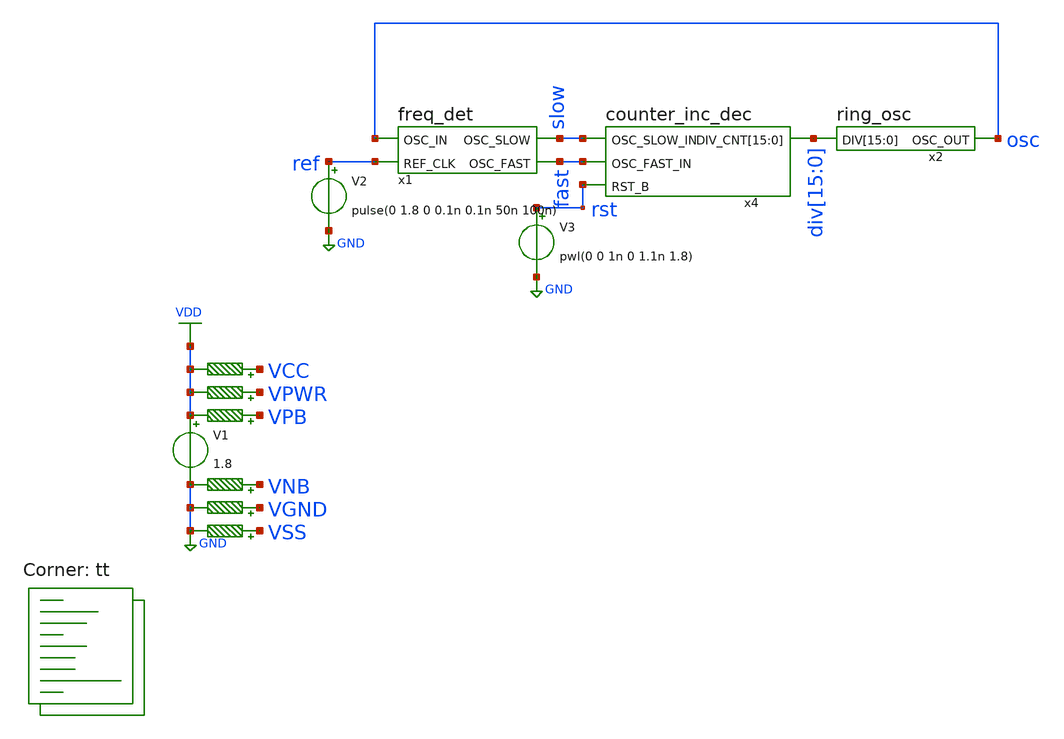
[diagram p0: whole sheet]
** sch_path: top.sch
**.subckt top
x1 slow fast osc ref freq_det
x2 div[15] div[14] div[13] div[12] div[11] div[10] div[9] div[8] div[7] div[6] div[5] div[4] div[3]
+ div[2] div[1] div[0] osc ring_osc
x4 div[15] div[14] div[13] div[12] div[11] div[10] div[9] div[8] div[7] div[6] div[5] div[4] div[3]
+ div[2] div[1] div[0] fast slow rst counter_inc_dec
V2 ref GND pulse(0 1.8 0 0.1n 0.1n 50n 100n)
V3 rst GND pwl(0 0 1n 0 1.1n 1.8)
V1 VDD GND 1.8
R1 VPB VDD 0.01 m=1
R2 VPWR VDD 0.01 m=1
R3 VCC VDD 0.01 m=1
R4 VNB GND 0.01 m=1
R5 VGND GND 0.01 m=1
R6 VSS GND 0.01 m=1
**** begin user architecture code
.lib $::SKYWATER_MODELS/sky130.lib.spice tt


.include /usr/local/share/pdk/sky130A/libs.ref/sky130_fd_sc_hd/spice/sky130_fd_sc_hd.spice tt
.control
  save all
  tran 1n 10u
  write top.raw
  quit 0
.endc


**** end user architecture code
**.ends

* expanding   symbol:  freq_det.sym # of pins=4
** sym_path: freq_det.sym
** sch_path: freq_det.sch
.subckt freq_det OSC_SLOW OSC_FAST OSC_IN REF_CLK
*.ipin OSC_IN
*.ipin REF_CLK
*.opin OSC_FAST
*.opin OSC_SLOW
x8 OSC_IN VGND VNB VPB VPWR net1 sky130_fd_sc_hd__buf_1
x7 net4 net5 VGND VNB VPB VPWR OSC_FAST sky130_fd_sc_hd__or2_0
x11 net9 net10 VGND VNB VPB VPWR net5 sky130_fd_sc_hd__and2_0
x19 net1 VDD net2 VGND VNB VPB VPWR net10 sky130_fd_sc_hd__dfrtp_1
x1 net1 VDD net2 VGND VNB VPB VPWR net9 sky130_fd_sc_hd__dfrtn_1
x2 net1 VDD net3 VGND VNB VPB VPWR net11 sky130_fd_sc_hd__dfrtp_1
x3 net1 VDD net3 VGND VNB VPB VPWR net12 sky130_fd_sc_hd__dfrtn_1
x4 net2 VGND VNB VPB VPWR net3 sky130_fd_sc_hd__inv_1
x5 net12 net11 VGND VNB VPB VPWR net4 sky130_fd_sc_hd__and2_0
x9 net13 net14 VGND VNB VPB VPWR net8 sky130_fd_sc_hd__and2_0
x10 net2 VDD net1 VGND VNB VPB VPWR net14 sky130_fd_sc_hd__dfrtp_1
x12 net2 VDD net1 VGND VNB VPB VPWR net13 sky130_fd_sc_hd__dfrtn_1
x15 net2 VDD net6 VGND VNB VPB VPWR net15 sky130_fd_sc_hd__dfrtp_1
x20 net2 VDD net6 VGND VNB VPB VPWR net16 sky130_fd_sc_hd__dfrtn_1
x21 net1 VGND VNB VPB VPWR net6 sky130_fd_sc_hd__inv_1
x22 net16 net15 VGND VNB VPB VPWR net7 sky130_fd_sc_hd__and2_0
x6 net7 net8 VGND VNB VPB VPWR OSC_SLOW sky130_fd_sc_hd__nor2_1
x23 REF_CLK VGND VNB VPB VPWR net2 sky130_fd_sc_hd__buf_1
R1 VPB VDD 0.01 m=1
R2 VPWR VDD 0.01 m=1
R3 VCC VDD 0.01 m=1
R4 VNB GND 0.01 m=1
R5 VGND GND 0.01 m=1
R6 VSS GND 0.01 m=1
.ends


* expanding   symbol:  ring_osc.sym # of pins=2
** sym_path: ring_osc.sym
** sch_path: ring_osc.sch
.subckt ring_osc DIV[15] DIV[14] DIV[13] DIV[12] DIV[11] DIV[10] DIV[9] DIV[8] DIV[7] DIV[6] DIV[5]
+ DIV[4] DIV[3] DIV[2] DIV[1] DIV[0] OSC_OUT
*.opin OSC_OUT
*.ipin
*+ DIV[15],DIV[14],DIV[13],DIV[12],DIV[11],DIV[10],DIV[9],DIV[8],DIV[7],DIV[6],DIV[5],DIV[4],DIV[3],DIV[2],DIV[1],DIV[0]
x4 net1 VGND VNB VPB VPWR net2 sky130_fd_sc_hd__clkdlybuf4s25_1
x5 net3 VGND VNB VPB VPWR net4 sky130_fd_sc_hd__clkdlybuf4s50_1
x6 net1 net2 DIV[0] VGND VNB VPB VPWR net3 sky130_fd_sc_hd__mux2i_1
x1 net3 net4 DIV[1] VGND VNB VPB VPWR net5 sky130_fd_sc_hd__mux2i_1
x2 net5 net7 DIV[2] VGND VNB VPB VPWR net8 sky130_fd_sc_hd__mux2i_1
x3 net5 VGND VNB VPB VPWR net6 sky130_fd_sc_hd__clkdlybuf4s25_1
x7 net6 VGND VNB VPB VPWR net7 sky130_fd_sc_hd__clkdlybuf4s50_1
x8 net8 VGND VNB VPB VPWR net10 sky130_fd_sc_hd__clkdlybuf4s50_1
x9 net10 VGND VNB VPB VPWR net9 sky130_fd_sc_hd__clkdlybuf4s50_1
x10 net8 net9 DIV[3] VGND VNB VPB VPWR net11 sky130_fd_sc_hd__mux2i_1
x11 net11 VGND VNB VPB VPWR net12 sky130_fd_sc_hd__clkdlybuf4s25_1
x12 net12 VGND VNB VPB VPWR net13 sky130_fd_sc_hd__clkdlybuf4s50_1
x13 net13 VGND VNB VPB VPWR net14 sky130_fd_sc_hd__clkdlybuf4s50_1
x14 net11 net14 DIV[4] VGND VNB VPB VPWR net15 sky130_fd_sc_hd__mux2i_1
x15 net15 VGND VNB VPB VPWR net18 sky130_fd_sc_hd__clkdlybuf4s50_1
x16 net18 VGND VNB VPB VPWR net17 sky130_fd_sc_hd__clkdlybuf4s50_1
x17 net17 VGND VNB VPB VPWR net16 sky130_fd_sc_hd__clkdlybuf4s50_1
x18 net15 net16 DIV[5] VGND VNB VPB VPWR net19 sky130_fd_sc_hd__mux2i_1
x19 net19 VGND VNB VPB VPWR net20 sky130_fd_sc_hd__clkdlybuf4s25_1
x20 net20 VGND VNB VPB VPWR net21 sky130_fd_sc_hd__clkdlybuf4s50_1
x21 net21 VGND VNB VPB VPWR net22 sky130_fd_sc_hd__clkdlybuf4s50_1
x22 net22 VGND VNB VPB VPWR net23 sky130_fd_sc_hd__clkdlybuf4s50_1
x23 net19 net23 DIV[6] VGND VNB VPB VPWR net24 sky130_fd_sc_hd__mux2i_1
x25 net28 VGND VNB VPB VPWR net27 sky130_fd_sc_hd__clkdlybuf4s50_1
x26 net27 VGND VNB VPB VPWR net26 sky130_fd_sc_hd__clkdlybuf4s50_1
x27 net26 VGND VNB VPB VPWR net25 sky130_fd_sc_hd__clkdlybuf4s50_1
x28 net24 net25 DIV[7] VGND VNB VPB VPWR net29 sky130_fd_sc_hd__mux2i_1
x24 net24 VGND VNB VPB VPWR net28 sky130_fd_sc_hd__clkdlybuf4s50_1
x29 net33 VGND VNB VPB VPWR net32 sky130_fd_sc_hd__clkdlybuf4s50_1
x30 net32 VGND VNB VPB VPWR net31 sky130_fd_sc_hd__clkdlybuf4s50_1
x31 net31 VGND VNB VPB VPWR net30 sky130_fd_sc_hd__clkdlybuf4s50_1
x32 net29 net30 DIV[8] VGND VNB VPB VPWR net35 sky130_fd_sc_hd__mux2i_1
x33 net34 VGND VNB VPB VPWR net33 sky130_fd_sc_hd__clkdlybuf4s50_1
x34 net29 VGND VNB VPB VPWR net34 sky130_fd_sc_hd__clkdlybuf4s25_1
x35 net39 VGND VNB VPB VPWR net38 sky130_fd_sc_hd__clkdlybuf4s50_1
x36 net38 VGND VNB VPB VPWR net37 sky130_fd_sc_hd__clkdlybuf4s50_1
x37 net37 VGND VNB VPB VPWR net36 sky130_fd_sc_hd__clkdlybuf4s50_1
x38 net35 net36 DIV[9] VGND VNB VPB VPWR net41 sky130_fd_sc_hd__mux2i_1
x39 net40 VGND VNB VPB VPWR net39 sky130_fd_sc_hd__clkdlybuf4s50_1
x41 net46 VGND VNB VPB VPWR net45 sky130_fd_sc_hd__clkdlybuf4s50_1
x42 net45 VGND VNB VPB VPWR net44 sky130_fd_sc_hd__clkdlybuf4s50_1
x43 net44 VGND VNB VPB VPWR net43 sky130_fd_sc_hd__clkdlybuf4s50_1
x44 net41 net42 DIV[10] VGND VNB VPB VPWR net48 sky130_fd_sc_hd__mux2i_1
x45 net47 VGND VNB VPB VPWR net46 sky130_fd_sc_hd__clkdlybuf4s50_1
x46 net41 VGND VNB VPB VPWR net47 sky130_fd_sc_hd__clkdlybuf4s25_1
x47 net43 VGND VNB VPB VPWR net42 sky130_fd_sc_hd__clkdlybuf4s50_1
x48 net53 VGND VNB VPB VPWR net52 sky130_fd_sc_hd__clkdlybuf4s50_1
x49 net52 VGND VNB VPB VPWR net51 sky130_fd_sc_hd__clkdlybuf4s50_1
x50 net51 VGND VNB VPB VPWR net50 sky130_fd_sc_hd__clkdlybuf4s50_1
x51 net48 net49 DIV[11] VGND VNB VPB VPWR net55 sky130_fd_sc_hd__mux2i_1
x52 net54 VGND VNB VPB VPWR net53 sky130_fd_sc_hd__clkdlybuf4s50_1
x54 net50 VGND VNB VPB VPWR net49 sky130_fd_sc_hd__clkdlybuf4s50_1
x55 net61 VGND VNB VPB VPWR net60 sky130_fd_sc_hd__clkdlybuf4s50_1
x56 net60 VGND VNB VPB VPWR net59 sky130_fd_sc_hd__clkdlybuf4s50_1
x57 net59 VGND VNB VPB VPWR net58 sky130_fd_sc_hd__clkdlybuf4s50_1
x58 net55 net56 DIV[12] VGND VNB VPB VPWR net63 sky130_fd_sc_hd__mux2i_1
x59 net62 VGND VNB VPB VPWR net61 sky130_fd_sc_hd__clkdlybuf4s50_1
x60 net55 VGND VNB VPB VPWR net62 sky130_fd_sc_hd__clkdlybuf4s25_1
x61 net58 VGND VNB VPB VPWR net57 sky130_fd_sc_hd__clkdlybuf4s50_1
x62 net57 VGND VNB VPB VPWR net56 sky130_fd_sc_hd__clkdlybuf4s50_1
x63 net69 VGND VNB VPB VPWR net68 sky130_fd_sc_hd__clkdlybuf4s50_1
x64 net68 VGND VNB VPB VPWR net67 sky130_fd_sc_hd__clkdlybuf4s50_1
x65 net67 VGND VNB VPB VPWR net66 sky130_fd_sc_hd__clkdlybuf4s50_1
x66 net63 net64 DIV[13] VGND VNB VPB VPWR net71 sky130_fd_sc_hd__mux2i_1
x67 net70 VGND VNB VPB VPWR net69 sky130_fd_sc_hd__clkdlybuf4s50_1
x69 net66 VGND VNB VPB VPWR net65 sky130_fd_sc_hd__clkdlybuf4s50_1
x70 net65 VGND VNB VPB VPWR net64 sky130_fd_sc_hd__clkdlybuf4s50_1
x71 net78 VGND VNB VPB VPWR net77 sky130_fd_sc_hd__clkdlybuf4s50_1
x72 net77 VGND VNB VPB VPWR net76 sky130_fd_sc_hd__clkdlybuf4s50_1
x73 net76 VGND VNB VPB VPWR net75 sky130_fd_sc_hd__clkdlybuf4s50_1
x74 net71 net72 DIV[14] VGND VNB VPB VPWR net80 sky130_fd_sc_hd__mux2i_1
x75 net79 VGND VNB VPB VPWR net78 sky130_fd_sc_hd__clkdlybuf4s50_1
x76 net71 VGND VNB VPB VPWR net79 sky130_fd_sc_hd__clkdlybuf4s25_1
x77 net75 VGND VNB VPB VPWR net74 sky130_fd_sc_hd__clkdlybuf4s50_1
x78 net74 VGND VNB VPB VPWR net73 sky130_fd_sc_hd__clkdlybuf4s50_1
x79 net73 VGND VNB VPB VPWR net72 sky130_fd_sc_hd__clkdlybuf4s50_1
x80 net82 VGND VNB VPB VPWR net83 sky130_fd_sc_hd__clkdlybuf4s50_1
x81 net83 VGND VNB VPB VPWR net84 sky130_fd_sc_hd__clkdlybuf4s50_1
x82 net84 VGND VNB VPB VPWR net85 sky130_fd_sc_hd__clkdlybuf4s50_1
x83 net80 net88 DIV[15] VGND VNB VPB VPWR OSC_OUT sky130_fd_sc_hd__mux2i_1
x84 net81 VGND VNB VPB VPWR net82 sky130_fd_sc_hd__clkdlybuf4s50_1
x86 net85 VGND VNB VPB VPWR net86 sky130_fd_sc_hd__clkdlybuf4s50_1
x87 net86 VGND VNB VPB VPWR net87 sky130_fd_sc_hd__clkdlybuf4s50_1
x88 net87 VGND VNB VPB VPWR net88 sky130_fd_sc_hd__clkdlybuf4s50_1
x89 OSC_OUT VGND VNB VPB VPWR net1 sky130_fd_sc_hd__clkinv_1
x40 net35 VGND VNB VPB VPWR net40 sky130_fd_sc_hd__clkdlybuf4s50_1
x53 net48 VGND VNB VPB VPWR net54 sky130_fd_sc_hd__clkdlybuf4s50_1
x68 net63 VGND VNB VPB VPWR net70 sky130_fd_sc_hd__clkdlybuf4s50_1
x85 net80 VGND VNB VPB VPWR net81 sky130_fd_sc_hd__clkdlybuf4s50_1
.ends


* expanding   symbol:  counter_inc_dec.sym # of pins=4
** sym_path: counter_inc_dec.sym
** sch_path: counter_inc_dec.sch
.subckt counter_inc_dec DIV_CNT[15] DIV_CNT[14] DIV_CNT[13] DIV_CNT[12] DIV_CNT[11] DIV_CNT[10]
+ DIV_CNT[9] DIV_CNT[8] DIV_CNT[7] DIV_CNT[6] DIV_CNT[5] DIV_CNT[4] DIV_CNT[3] DIV_CNT[2] DIV_CNT[1] DIV_CNT[0]
+ OSC_FAST_IN OSC_SLOW_IN RST_B
*.ipin OSC_FAST_IN
*.ipin OSC_SLOW_IN
*.ipin RST_B
*.opin
*+ DIV_CNT[15],DIV_CNT[14],DIV_CNT[13],DIV_CNT[12],DIV_CNT[11],DIV_CNT[10],DIV_CNT[9],DIV_CNT[8],DIV_CNT[7],DIV_CNT[6],DIV_CNT[5],DIV_CNT[4],DIV_CNT[3],DIV_CNT[2],DIV_CNT[1],DIV_CNT[0]
x1 net11 net10 DIV_CNT[1] DIV_CNT[0] net2 net9 RST_B add_sub_bit
x3 OSC_FAST_IN OSC_SLOW_IN VGND VNB VPB VPWR net1 sky130_fd_sc_hd__or2_0
x5 net1 net9 RST_B VGND VNB VPB VPWR net3 net6 sky130_fd_sc_hd__dfrbp_1
x8 net6 net5 VGND VNB VPB VPWR net8 sky130_fd_sc_hd__and2_0
x9 net3 net4 VGND VNB VPB VPWR net7 sky130_fd_sc_hd__and2_0
x10 net8 net7 VGND VNB VPB VPWR net10 sky130_fd_sc_hd__or2_0
x25 net1 OSC_FAST_IN RST_B VGND VNB VPB VPWR net5 sky130_fd_sc_hd__dfrtp_1
x6 net1 OSC_SLOW_IN RST_B VGND VNB VPB VPWR net4 sky130_fd_sc_hd__dfrtp_1
x7 net12 net10 DIV_CNT[2] DIV_CNT[1] net11 net9 RST_B add_sub_bit
x11 net13 net10 DIV_CNT[3] DIV_CNT[2] net12 net9 RST_B add_sub_bit
x12 net14 net10 DIV_CNT[4] DIV_CNT[3] net13 net9 RST_B add_sub_bit
x13 net15 net10 DIV_CNT[5] DIV_CNT[4] net14 net9 RST_B add_sub_bit
x14 net16 net10 DIV_CNT[6] DIV_CNT[5] net15 net9 RST_B add_sub_bit
x15 net17 net10 DIV_CNT[7] DIV_CNT[6] net16 net9 RST_B add_sub_bit
x16 net18 net10 DIV_CNT[8] DIV_CNT[7] net17 net9 RST_B add_sub_bit
x17 net19 net10 DIV_CNT[9] DIV_CNT[8] net18 net9 RST_B add_sub_bit
x18 net20 net10 DIV_CNT[10] DIV_CNT[9] net19 net9 RST_B add_sub_bit
x19 net21 net10 DIV_CNT[11] DIV_CNT[10] net20 net9 RST_B add_sub_bit
x20 net22 net10 DIV_CNT[12] DIV_CNT[11] net21 net9 RST_B add_sub_bit
x21 net23 net10 DIV_CNT[13] DIV_CNT[12] net22 net9 RST_B add_sub_bit
x22 net24 net10 DIV_CNT[14] DIV_CNT[13] net23 net9 RST_B add_sub_bit
x23 net26 net10 DIV_CNT[15] DIV_CNT[14] net24 net9 RST_B add_sub_bit
* noconn #net26
x4 OSC_SLOW_IN net9 VGND VNB VPB VPWR net25 sky130_fd_sc_hd__nand2b_1
x24 OSC_FAST_IN net25 VGND VNB VPB VPWR net9 sky130_fd_sc_hd__nand2b_1
* tap: DIV_CNT[15:0] --> DIV_CNT[0]
* tap: DIV_CNT[15:0] --> DIV_CNT[1]
* tap: DIV_CNT[15:0] --> DIV_CNT[2]
* tap: DIV_CNT[15:0] --> DIV_CNT[3]
* tap: DIV_CNT[15:0] --> DIV_CNT[4]
* tap: DIV_CNT[15:0] --> DIV_CNT[5]
* tap: DIV_CNT[15:0] --> DIV_CNT[6]
* tap: DIV_CNT[15:0] --> DIV_CNT[7]
* tap: DIV_CNT[15:0] --> DIV_CNT[8]
* tap: DIV_CNT[15:0] --> DIV_CNT[9]
* tap: DIV_CNT[15:0] --> DIV_CNT[10]
* tap: DIV_CNT[15:0] --> DIV_CNT[11]
* tap: DIV_CNT[15:0] --> DIV_CNT[12]
* tap: DIV_CNT[15:0] --> DIV_CNT[13]
* tap: DIV_CNT[15:0] --> DIV_CNT[14]
* tap: DIV_CNT[15:0] --> DIV_CNT[15]
x26 net1 net2 RST_B VGND VNB VPB VPWR DIV_CNT[0] net2 sky130_fd_sc_hd__dfsbp_1
.ends


* expanding   symbol:  add_sub_bit.sym # of pins=7
** sym_path: add_sub_bit.sym
** sch_path: add_sub_bit.sch
.subckt add_sub_bit Q_N_OUT S_D Q_OUT Q_IN Q_N_IN S_CLK RST_B
*.ipin S_D
*.ipin S_CLK
*.opin Q_OUT
*.opin Q_N_OUT
*.ipin RST_B
*.ipin Q_N_IN
*.ipin Q_IN
x2 Q_N_OUT Q_OUT S_D VGND VNB VPB VPWR net2 sky130_fd_sc_hd__mux2_1
x3 Q_IN Q_N_IN S_CLK VGND VNB VPB VPWR net1 sky130_fd_sc_hd__mux2_1
x4 net1 net2 RST_B VGND VNB VPB VPWR Q_OUT Q_N_OUT sky130_fd_sc_hd__dfrbp_1
.ends

.GLOBAL GND
.GLOBAL VDD
**** begin user architecture code


.GLOBAL VDD
.GLOBAL GND
.GLOBAL VCC
.GLOBAL VPWR
.GLOBAL VPB
.GLOBAL VNB
.GLOBAL VGND
.GLOBAL VSS


**** end user architecture code
.end
